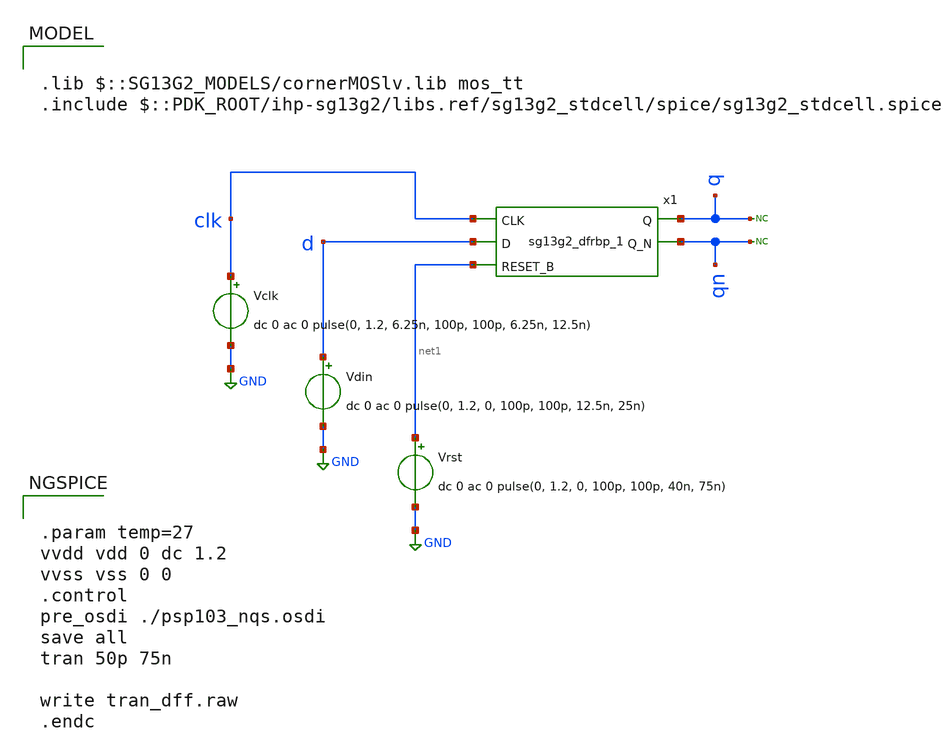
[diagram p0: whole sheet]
** sch_path: Combined Design/design_data/xschem/dff_tb.sch

.lib $::SG13G2_MODELS/cornerMOSlv.lib mos_tt
.include $::PDK_ROOT/ihp-sg13g2/libs.ref/sg13g2_stdcell/spice/sg13g2_stdcell.spice

**.subckt dff_tb
x1 q qn clk d net1 VDD VSS sg13g2_dfrbp_1
Vclk clk GND dc 0 ac 0 pulse(0, 1.2, 6.25n, 100p, 100p, 6.25n, 12.5n)
Vdin d GND dc 0 ac 0 pulse(0, 1.2, 0, 100p, 100p, 12.5n, 25n)
* noconn q
* noconn qn
Vrst net1 GND dc 0 ac 0 pulse(0, 1.2, 0, 100p, 100p, 40n, 75n)
**** begin user architecture code


.param temp=27
vvdd vdd 0 dc 1.2
vvss vss 0 0
.control
pre_osdi ./psp103_nqs.osdi
save all
tran 50p 75n

write tran_dff.raw
.endc


**** end user architecture code
**.ends

* expanding   symbol:  sg13g2_stdcells/sg13g2_dfrbp_1.sym # of pins=5
** sym_path: sg13g2_stdcells/sg13g2_dfrbp_1.sym
** sch_path: sg13g2_stdcells/sg13g2_dfrbp_1.sch
.subckt sg13g2_dfrbp_1 Q Q_N CLK D RESET_B VDD VSS
*.ipin D
*.ipin RESET_B
*.ipin CLK
*.opin Q
*.opin Q_N
*.iopin VDD
*.iopin VSS
XM1 Db D net10 VSS sg13_lv_nmos w=420.00n l=130.00n ng=1 m=1 mm_ok=1
XM2 net10 RESET_B VSS VSS sg13_lv_nmos w=420.00n l=130.00n ng=1 m=1 mm_ok=1
XM3 net1 clkneg net9 VSS sg13_lv_nmos w=420.00n l=130.00n ng=1 m=1 mm_ok=1
XM4 net9 net1 VSS VSS sg13_lv_nmos w=420.00n l=130.00n ng=1 m=1 mm_ok=1
XM5 net1 net1 net5 VSS sg13_lv_nmos w=420.00n l=130.00n ng=1 m=1 mm_ok=1
XM6 net5 RESET_B VSS VSS sg13_lv_nmos w=420.00n l=130.00n ng=1 m=1 mm_ok=1
XM7 Q_N net1 VSS VSS sg13_lv_nmos w=740.00n l=130.00n ng=1 m=1 mm_ok=1
XM8 net2 net1 VSS VSS sg13_lv_nmos w=740.00n l=130.00n ng=1 m=1 mm_ok=1
XM9 Q net2 VSS VSS sg13_lv_nmos w=740.00n l=130.00n ng=1 m=1 mm_ok=1
XM10 clkneg CLK VSS VSS sg13_lv_nmos w=740.00n l=130.00n ng=1 m=1 mm_ok=1
XM11 clkpos clkneg VSS VSS sg13_lv_nmos w=740.00n l=130.00n ng=1 m=1 mm_ok=1
XM12 Db clkneg net3 VSS sg13_lv_nmos w=420.00n l=130.00n ng=1 m=1 mm_ok=1
XM13 net3 clkpos net8 VSS sg13_lv_nmos w=420.00n l=130.00n ng=1 m=1 mm_ok=1
XM14 net8 net3 net4 VSS sg13_lv_nmos w=420.00n l=130.00n ng=1 m=1 mm_ok=1
XM15 net4 RESET_B VSS VSS sg13_lv_nmos w=420.00n l=130.00n ng=1 m=1 mm_ok=1
XM16 net3 net3 VSS VSS sg13_lv_nmos w=740.00n l=130.00n ng=1 m=1 mm_ok=1
XM17 net3 clkpos net1 VSS sg13_lv_nmos w=740.00n l=130.00n ng=1 m=1 mm_ok=1
XM18 Db RESET_B VDD VDD sg13_lv_pmos w=420.00n l=130.00n ng=1 m=1 mm_ok=1
XM19 Db D VDD VDD sg13_lv_pmos w=420.00n l=130.00n ng=1 m=1 mm_ok=1
XM20 net7 net1 VDD VDD sg13_lv_pmos w=420.00n l=130.00n ng=1 m=1 mm_ok=1
XM21 net1 clkpos net7 VDD sg13_lv_pmos w=420.00n l=130.00n ng=1 m=1 mm_ok=1
XM22 net1 net1 VDD VDD sg13_lv_pmos w=420.00n l=130.00n ng=1 m=1 mm_ok=1
XM23 net1 RESET_B VDD VDD sg13_lv_pmos w=420.00n l=130.00n ng=1 m=1 mm_ok=1
XM24 Q_N net1 VDD VDD sg13_lv_pmos w=1.12u l=130.00n ng=1 m=1 mm_ok=1
XM25 net2 net1 VDD VDD sg13_lv_pmos w=1.12u l=130.00n ng=1 m=1 mm_ok=1
XM26 Q net2 VDD VDD sg13_lv_pmos w=1.12u l=130.00n ng=1 m=1 mm_ok=1
XM27 clkneg CLK VDD VDD sg13_lv_pmos w=1.12u l=130.00n ng=1 m=1 mm_ok=1
XM28 clkpos clkneg VDD VDD sg13_lv_pmos w=1.12u l=130.00n ng=1 m=1 mm_ok=1
XM29 Db clkpos net3 VDD sg13_lv_pmos w=420.00n l=130.00n ng=1 m=1 mm_ok=1
XM30 net6 net3 VDD VDD sg13_lv_pmos w=420.00n l=130.00n ng=1 m=1 mm_ok=1
XM31 net3 clkneg net6 VDD sg13_lv_pmos w=420.00n l=130.00n ng=1 m=1 mm_ok=1
XM32 net3 RESET_B VDD VDD sg13_lv_pmos w=420.00n l=130.00n ng=1 m=1 mm_ok=1
XM33 net3 net3 VDD VDD sg13_lv_pmos w=1.000u l=130.00n ng=1 m=1 mm_ok=1
XM34 net3 clkneg net1 VDD sg13_lv_pmos w=1.000u l=130.00n ng=1 m=1 mm_ok=1
.ends

.GLOBAL GND
.end
